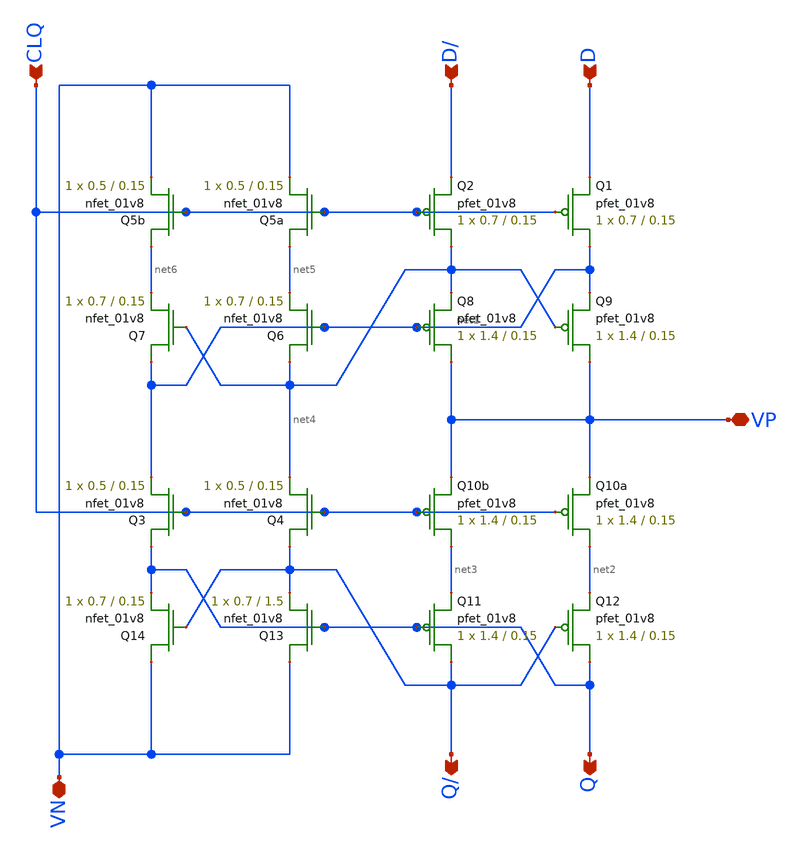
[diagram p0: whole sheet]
** sch_path: MADVLSI_MP2/Lay_CSRL.sch
**.subckt Lay_CSRL D/ D CLQ VP VN Q/ Q
*.ipin D/
*.ipin D
*.ipin CLQ
*.iopin VP
*.iopin VN
*.opin Q/
*.opin Q
XQ2 net4 CLQ D/ VDD sky130_fd_pr__pfet_01v8 L=0.15 W=0.7 nf=1 ad='int((nf+1)/2) * W/nf * 0.29' as='int((nf+2)/2) * W/nf * 0.29'
+ pd='2*int((nf+1)/2) * (W/nf + 0.29)' ps='2*int((nf+2)/2) * (W/nf + 0.29)' nrd='0.29 / W' nrs='0.29 / W'
+ sa=0 sb=0 sd=0 mult=1 m=1
XQ8 VP net1 net4 VDD sky130_fd_pr__pfet_01v8 L=0.15 W=1.4 nf=1 ad='int((nf+1)/2) * W/nf * 0.29' as='int((nf+2)/2) * W/nf * 0.29'
+ pd='2*int((nf+1)/2) * (W/nf + 0.29)' ps='2*int((nf+2)/2) * (W/nf + 0.29)' nrd='0.29 / W' nrs='0.29 / W'
+ sa=0 sb=0 sd=0 mult=1 m=1
XQ10b net3 CLQ VP VDD sky130_fd_pr__pfet_01v8 L=0.15 W=1.4 nf=1 ad='int((nf+1)/2) * W/nf * 0.29' as='int((nf+2)/2) * W/nf * 0.29'
+ pd='2*int((nf+1)/2) * (W/nf + 0.29)' ps='2*int((nf+2)/2) * (W/nf + 0.29)' nrd='0.29 / W' nrs='0.29 / W'
+ sa=0 sb=0 sd=0 mult=1 m=1
XQ11 Q/ Q net3 VDD sky130_fd_pr__pfet_01v8 L=0.15 W=1.4 nf=1 ad='int((nf+1)/2) * W/nf * 0.29' as='int((nf+2)/2) * W/nf * 0.29'
+ pd='2*int((nf+1)/2) * (W/nf + 0.29)' ps='2*int((nf+2)/2) * (W/nf + 0.29)' nrd='0.29 / W' nrs='0.29 / W'
+ sa=0 sb=0 sd=0 mult=1 m=1
XQ1 net1 CLQ D VDD sky130_fd_pr__pfet_01v8 L=0.15 W=0.7 nf=1 ad='int((nf+1)/2) * W/nf * 0.29' as='int((nf+2)/2) * W/nf * 0.29'
+ pd='2*int((nf+1)/2) * (W/nf + 0.29)' ps='2*int((nf+2)/2) * (W/nf + 0.29)' nrd='0.29 / W' nrs='0.29 / W'
+ sa=0 sb=0 sd=0 mult=1 m=1
XQ9 VP net4 net1 VDD sky130_fd_pr__pfet_01v8 L=0.15 W=1.4 nf=1 ad='int((nf+1)/2) * W/nf * 0.29' as='int((nf+2)/2) * W/nf * 0.29'
+ pd='2*int((nf+1)/2) * (W/nf + 0.29)' ps='2*int((nf+2)/2) * (W/nf + 0.29)' nrd='0.29 / W' nrs='0.29 / W'
+ sa=0 sb=0 sd=0 mult=1 m=1
XQ10a net2 CLQ VP VDD sky130_fd_pr__pfet_01v8 L=0.15 W=1.4 nf=1 ad='int((nf+1)/2) * W/nf * 0.29' as='int((nf+2)/2) * W/nf * 0.29'
+ pd='2*int((nf+1)/2) * (W/nf + 0.29)' ps='2*int((nf+2)/2) * (W/nf + 0.29)' nrd='0.29 / W' nrs='0.29 / W'
+ sa=0 sb=0 sd=0 mult=1 m=1
XQ12 Q Q/ net2 VDD sky130_fd_pr__pfet_01v8 L=0.15 W=1.4 nf=1 ad='int((nf+1)/2) * W/nf * 0.29' as='int((nf+2)/2) * W/nf * 0.29'
+ pd='2*int((nf+1)/2) * (W/nf + 0.29)' ps='2*int((nf+2)/2) * (W/nf + 0.29)' nrd='0.29 / W' nrs='0.29 / W'
+ sa=0 sb=0 sd=0 mult=1 m=1
XQ5a net5 CLQ VN GND sky130_fd_pr__nfet_01v8 L=0.15 W=0.5 nf=1 ad='int((nf+1)/2) * W/nf * 0.29' as='int((nf+2)/2) * W/nf * 0.29'
+ pd='2*int((nf+1)/2) * (W/nf + 0.29)' ps='2*int((nf+2)/2) * (W/nf + 0.29)' nrd='0.29 / W' nrs='0.29 / W'
+ sa=0 sb=0 sd=0 mult=1 m=1
XQ6 net4 net1 net5 GND sky130_fd_pr__nfet_01v8 L=0.15 W=0.7 nf=1 ad='int((nf+1)/2) * W/nf * 0.29' as='int((nf+2)/2) * W/nf * 0.29'
+ pd='2*int((nf+1)/2) * (W/nf + 0.29)' ps='2*int((nf+2)/2) * (W/nf + 0.29)' nrd='0.29 / W' nrs='0.29 / W'
+ sa=0 sb=0 sd=0 mult=1 m=1
XQ4 Q/ CLQ net4 GND sky130_fd_pr__nfet_01v8 L=0.15 W=0.5 nf=1 ad='int((nf+1)/2) * W/nf * 0.29' as='int((nf+2)/2) * W/nf * 0.29'
+ pd='2*int((nf+1)/2) * (W/nf + 0.29)' ps='2*int((nf+2)/2) * (W/nf + 0.29)' nrd='0.29 / W' nrs='0.29 / W'
+ sa=0 sb=0 sd=0 mult=1 m=1
XQ13 VN Q Q/ GND sky130_fd_pr__nfet_01v8 L=1.5 W=0.7 nf=1 ad='int((nf+1)/2) * W/nf * 0.29' as='int((nf+2)/2) * W/nf * 0.29'
+ pd='2*int((nf+1)/2) * (W/nf + 0.29)' ps='2*int((nf+2)/2) * (W/nf + 0.29)' nrd='0.29 / W' nrs='0.29 / W'
+ sa=0 sb=0 sd=0 mult=1 m=1
XQ5b net6 CLQ VN GND sky130_fd_pr__nfet_01v8 L=0.15 W=0.5 nf=1 ad='int((nf+1)/2) * W/nf * 0.29' as='int((nf+2)/2) * W/nf * 0.29'
+ pd='2*int((nf+1)/2) * (W/nf + 0.29)' ps='2*int((nf+2)/2) * (W/nf + 0.29)' nrd='0.29 / W' nrs='0.29 / W'
+ sa=0 sb=0 sd=0 mult=1 m=1
XQ7 net1 net4 net6 GND sky130_fd_pr__nfet_01v8 L=0.15 W=0.7 nf=1 ad='int((nf+1)/2) * W/nf * 0.29' as='int((nf+2)/2) * W/nf * 0.29'
+ pd='2*int((nf+1)/2) * (W/nf + 0.29)' ps='2*int((nf+2)/2) * (W/nf + 0.29)' nrd='0.29 / W' nrs='0.29 / W'
+ sa=0 sb=0 sd=0 mult=1 m=1
XQ3 Q CLQ net1 GND sky130_fd_pr__nfet_01v8 L=0.15 W=0.5 nf=1 ad='int((nf+1)/2) * W/nf * 0.29' as='int((nf+2)/2) * W/nf * 0.29'
+ pd='2*int((nf+1)/2) * (W/nf + 0.29)' ps='2*int((nf+2)/2) * (W/nf + 0.29)' nrd='0.29 / W' nrs='0.29 / W'
+ sa=0 sb=0 sd=0 mult=1 m=1
XQ14 VN Q/ Q GND sky130_fd_pr__nfet_01v8 L=0.15 W=0.7 nf=1 ad='int((nf+1)/2) * W/nf * 0.29' as='int((nf+2)/2) * W/nf * 0.29'
+ pd='2*int((nf+1)/2) * (W/nf + 0.29)' ps='2*int((nf+2)/2) * (W/nf + 0.29)' nrd='0.29 / W' nrs='0.29 / W'
+ sa=0 sb=0 sd=0 mult=1 m=1
**.ends
.end
